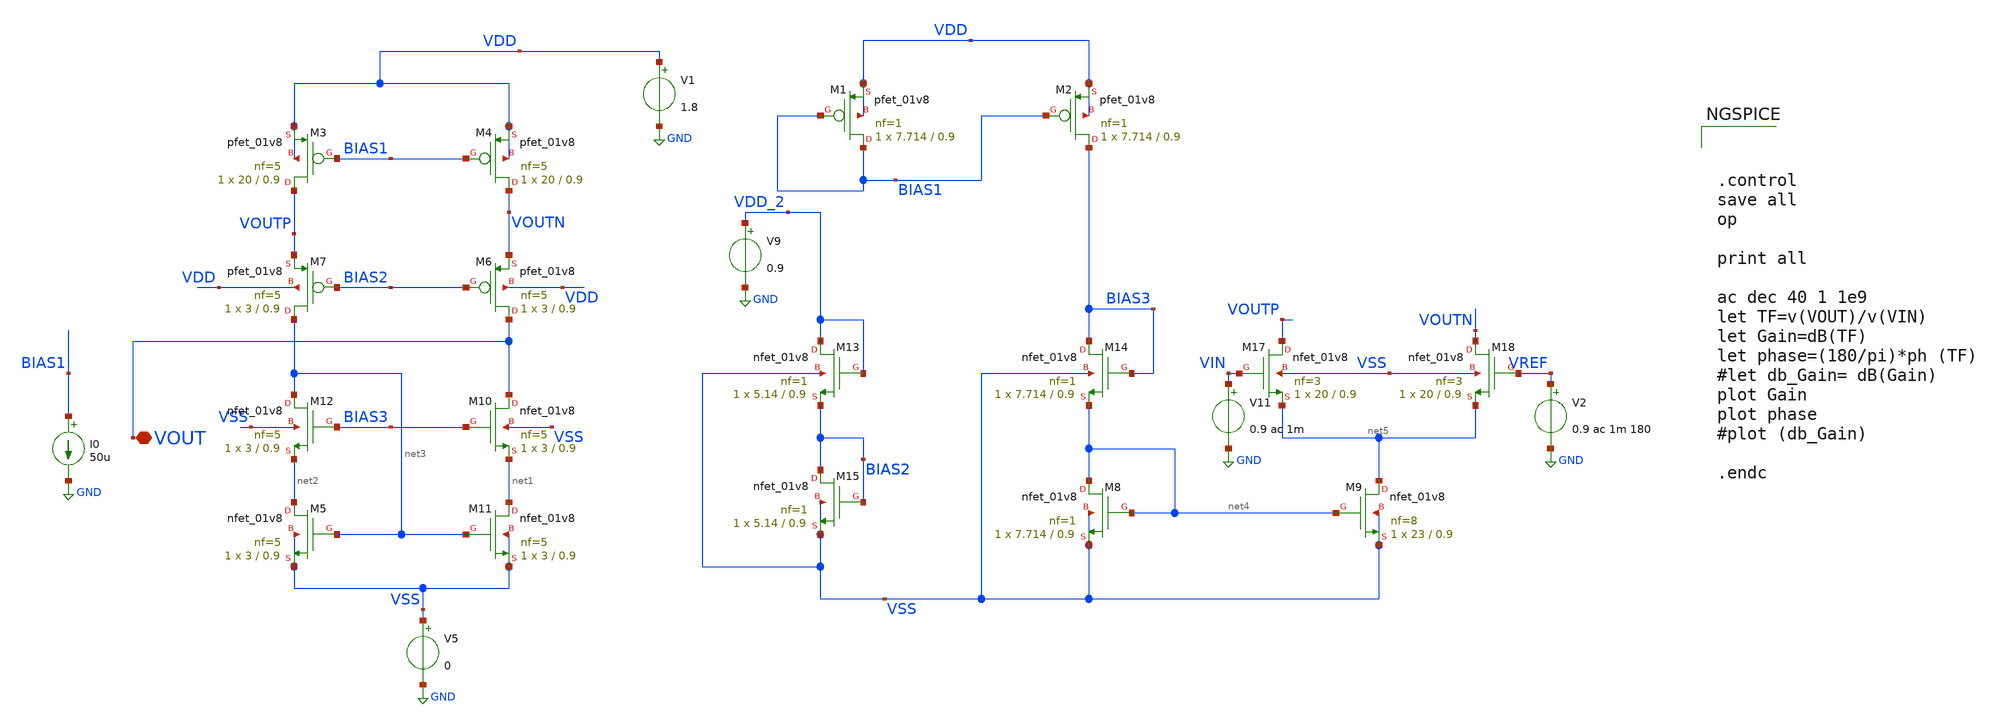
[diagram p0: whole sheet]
** sch_path: xschem/DC_DC_Converter_xschem/OTHERS/DC_DC_Converter0/Folded_OPAMP/Folded_OPAMP.sch
**.subckt Folded_OPAMP VOUT
*.iopin VOUT
V1 VDD GND 1.8
V5 VSS GND 0
I0 BIAS1 GND 50u
V9 VDD_2 GND 0.9
V11 VIN GND 0.9 ac 1m
XM3 VOUTP BIAS1 VDD VDD sky130_fd_pr__pfet_01v8 L=0.9 W=20 nf=5 ad='int((nf+1)/2) * W/nf * 0.29' as='int((nf+2)/2) * W/nf * 0.29'
+ pd='2*int((nf+1)/2) * (W/nf + 0.29)' ps='2*int((nf+2)/2) * (W/nf + 0.29)' nrd='0.29 / W' nrs='0.29 / W'
+ sa=0 sb=0 sd=0 mult=1 m=1
XM4 VOUTN BIAS1 VDD VDD sky130_fd_pr__pfet_01v8 L=0.9 W=20 nf=5 ad='int((nf+1)/2) * W/nf * 0.29' as='int((nf+2)/2) * W/nf * 0.29'
+ pd='2*int((nf+1)/2) * (W/nf + 0.29)' ps='2*int((nf+2)/2) * (W/nf + 0.29)' nrd='0.29 / W' nrs='0.29 / W'
+ sa=0 sb=0 sd=0 mult=1 m=1
XM6 VOUT BIAS2 VOUTN VDD sky130_fd_pr__pfet_01v8 L=0.9 W=3 nf=5 ad='int((nf+1)/2) * W/nf * 0.29' as='int((nf+2)/2) * W/nf * 0.29'
+ pd='2*int((nf+1)/2) * (W/nf + 0.29)' ps='2*int((nf+2)/2) * (W/nf + 0.29)' nrd='0.29 / W' nrs='0.29 / W'
+ sa=0 sb=0 sd=0 mult=1 m=1
XM7 net3 BIAS2 VOUTP VDD sky130_fd_pr__pfet_01v8 L=0.9 W=3 nf=5 ad='int((nf+1)/2) * W/nf * 0.29' as='int((nf+2)/2) * W/nf * 0.29'
+ pd='2*int((nf+1)/2) * (W/nf + 0.29)' ps='2*int((nf+2)/2) * (W/nf + 0.29)' nrd='0.29 / W' nrs='0.29 / W'
+ sa=0 sb=0 sd=0 mult=1 m=1
XM13 VDD_2 VDD_2 BIAS2 VSS sky130_fd_pr__nfet_01v8 L=0.9 W=5.14 nf=1 ad='int((nf+1)/2) * W/nf * 0.29'
+ as='int((nf+2)/2) * W/nf * 0.29' pd='2*int((nf+1)/2) * (W/nf + 0.29)' ps='2*int((nf+2)/2) * (W/nf + 0.29)'
+ nrd='0.29 / W' nrs='0.29 / W' sa=0 sb=0 sd=0 mult=1 m=1
XM14 BIAS3 BIAS3 net4 VSS sky130_fd_pr__nfet_01v8 L=0.9 W=7.714 nf=1 ad='int((nf+1)/2) * W/nf * 0.29'
+ as='int((nf+2)/2) * W/nf * 0.29' pd='2*int((nf+1)/2) * (W/nf + 0.29)' ps='2*int((nf+2)/2) * (W/nf + 0.29)'
+ nrd='0.29 / W' nrs='0.29 / W' sa=0 sb=0 sd=0 mult=1 m=1
XM15 BIAS2 BIAS2 VSS VSS sky130_fd_pr__nfet_01v8 L=0.9 W=5.14 nf=1 ad='int((nf+1)/2) * W/nf * 0.29' as='int((nf+2)/2) * W/nf * 0.29'
+ pd='2*int((nf+1)/2) * (W/nf + 0.29)' ps='2*int((nf+2)/2) * (W/nf + 0.29)' nrd='0.29 / W' nrs='0.29 / W'
+ sa=0 sb=0 sd=0 mult=1 m=1
XM17 VOUTP VIN net5 VSS sky130_fd_pr__nfet_01v8 L=0.9 W=20 nf=3 ad='int((nf+1)/2) * W/nf * 0.29' as='int((nf+2)/2) * W/nf * 0.29'
+ pd='2*int((nf+1)/2) * (W/nf + 0.29)' ps='2*int((nf+2)/2) * (W/nf + 0.29)' nrd='0.29 / W' nrs='0.29 / W'
+ sa=0 sb=0 sd=0 mult=1 m=1
XM18 VOUTN VREF net5 VSS sky130_fd_pr__nfet_01v8 L=0.9 W=20 nf=3 ad='int((nf+1)/2) * W/nf * 0.29' as='int((nf+2)/2) * W/nf * 0.29'
+ pd='2*int((nf+1)/2) * (W/nf + 0.29)' ps='2*int((nf+2)/2) * (W/nf + 0.29)' nrd='0.29 / W' nrs='0.29 / W'
+ sa=0 sb=0 sd=0 mult=1 m=1
XM10 VOUT BIAS3 net1 VSS sky130_fd_pr__nfet_01v8 L=0.9 W=3 nf=5 ad='int((nf+1)/2) * W/nf * 0.29' as='int((nf+2)/2) * W/nf * 0.29'
+ pd='2*int((nf+1)/2) * (W/nf + 0.29)' ps='2*int((nf+2)/2) * (W/nf + 0.29)' nrd='0.29 / W' nrs='0.29 / W'
+ sa=0 sb=0 sd=0 mult=1 m=1
XM12 net3 BIAS3 net2 VSS sky130_fd_pr__nfet_01v8 L=0.9 W=3 nf=5 ad='int((nf+1)/2) * W/nf * 0.29' as='int((nf+2)/2) * W/nf * 0.29'
+ pd='2*int((nf+1)/2) * (W/nf + 0.29)' ps='2*int((nf+2)/2) * (W/nf + 0.29)' nrd='0.29 / W' nrs='0.29 / W'
+ sa=0 sb=0 sd=0 mult=1 m=1
XM8 net4 net4 VSS VSS sky130_fd_pr__nfet_01v8 L=0.9 W=7.714 nf=1 ad='int((nf+1)/2) * W/nf * 0.29' as='int((nf+2)/2) * W/nf * 0.29'
+ pd='2*int((nf+1)/2) * (W/nf + 0.29)' ps='2*int((nf+2)/2) * (W/nf + 0.29)' nrd='0.29 / W' nrs='0.29 / W'
+ sa=0 sb=0 sd=0 mult=1 m=1
XM9 net5 net4 VSS VSS sky130_fd_pr__nfet_01v8 L=0.9 W=23 nf=8 ad='int((nf+1)/2) * W/nf * 0.29' as='int((nf+2)/2) * W/nf * 0.29'
+ pd='2*int((nf+1)/2) * (W/nf + 0.29)' ps='2*int((nf+2)/2) * (W/nf + 0.29)' nrd='0.29 / W' nrs='0.29 / W'
+ sa=0 sb=0 sd=0 mult=1 m=1
XM5 net2 net3 VSS VSS sky130_fd_pr__nfet_01v8 L=0.9 W=3 nf=5 ad='int((nf+1)/2) * W/nf * 0.29' as='int((nf+2)/2) * W/nf * 0.29'
+ pd='2*int((nf+1)/2) * (W/nf + 0.29)' ps='2*int((nf+2)/2) * (W/nf + 0.29)' nrd='0.29 / W' nrs='0.29 / W'
+ sa=0 sb=0 sd=0 mult=1 m=1
XM11 net1 net3 VSS VSS sky130_fd_pr__nfet_01v8 L=0.9 W=3 nf=5 ad='int((nf+1)/2) * W/nf * 0.29' as='int((nf+2)/2) * W/nf * 0.29'
+ pd='2*int((nf+1)/2) * (W/nf + 0.29)' ps='2*int((nf+2)/2) * (W/nf + 0.29)' nrd='0.29 / W' nrs='0.29 / W'
+ sa=0 sb=0 sd=0 mult=1 m=1
XM1 BIAS1 BIAS1 VDD VDD sky130_fd_pr__pfet_01v8 L=0.9 W=7.714 nf=1 ad='int((nf+1)/2) * W/nf * 0.29' as='int((nf+2)/2) * W/nf * 0.29'
+ pd='2*int((nf+1)/2) * (W/nf + 0.29)' ps='2*int((nf+2)/2) * (W/nf + 0.29)' nrd='0.29 / W' nrs='0.29 / W'
+ sa=0 sb=0 sd=0 mult=1 m=1
XM2 BIAS3 BIAS1 VDD VDD sky130_fd_pr__pfet_01v8 L=0.9 W=7.714 nf=1 ad='int((nf+1)/2) * W/nf * 0.29' as='int((nf+2)/2) * W/nf * 0.29'
+ pd='2*int((nf+1)/2) * (W/nf + 0.29)' ps='2*int((nf+2)/2) * (W/nf + 0.29)' nrd='0.29 / W' nrs='0.29 / W'
+ sa=0 sb=0 sd=0 mult=1 m=1
V2 VREF GND 0.9 ac 1m 180
**** begin user architecture code

** opencircuitdesign pdks install
.lib $::SKYWATER_MODELS/sky130.lib.spice tt





.control
save all
op

print all

ac dec 40 1 1e9
let TF=v(VOUT)/v(VIN)
let Gain=dB(TF)
let phase=(180/pi)*ph (TF)
#let db_Gain= dB(Gain)
plot Gain
plot phase
#plot (db_Gain)

.endc


**** end user architecture code
**.ends
.GLOBAL GND
.end
